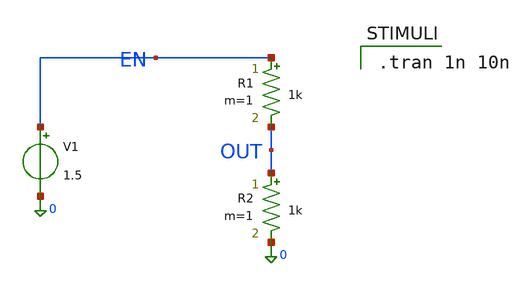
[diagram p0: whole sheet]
** sch_path: doc/claude/casemode_batch/eyeball_en_goal.sch
**.subckt eyeball_en_goal
V1 EN 0 1.5
R1 EN OUT 1k m=1
R2 OUT 0 1k m=1
**** begin user architecture code

.tran 1n 10n


**** end user architecture code
**.ends
.end
